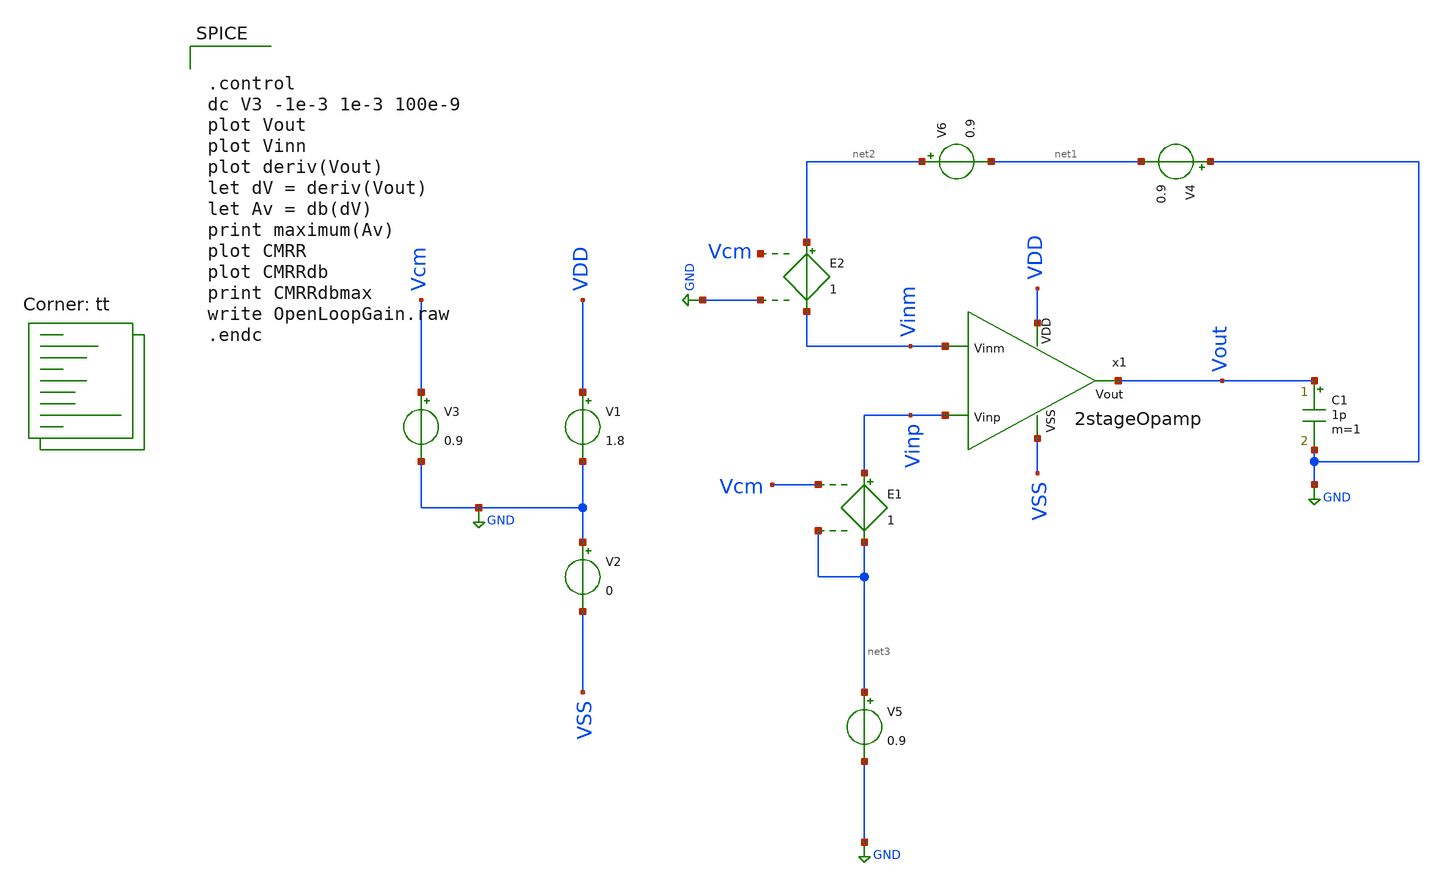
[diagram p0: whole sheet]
** sch_path: xschem/TestBenches/OpenLoopGain.sch
**.subckt OpenLoopGain
V1 VDD GND 1.8
V2 GND VSS 0
V3 Vcm GND 0.9
x1 VDD Vinm Vinp Vout VSS 2stageOpamp
E1 Vinp net3 Vcm net3 1
E2 net2 Vinm Vcm GND 1
V4 GND net1 0.9
C1 Vout GND 1p m=1
V5 net3 GND 0.9
V6 net2 net1 0.9
**** begin user architecture code


.control
dc V3 -1e-3 1e-3 100e-9
plot Vout
plot Vinn
plot deriv(Vout)
let dV = deriv(Vout)
let Av = db(dV)
print maximum(Av)
plot CMRR
plot CMRRdb
print CMRRdbmax
write OpenLoopGain.raw
.endc



.lib $::SKYWATER_MODELS/sky130.lib.spice tt
**** end user architecture code
**.ends
.GLOBAL GND
.end
